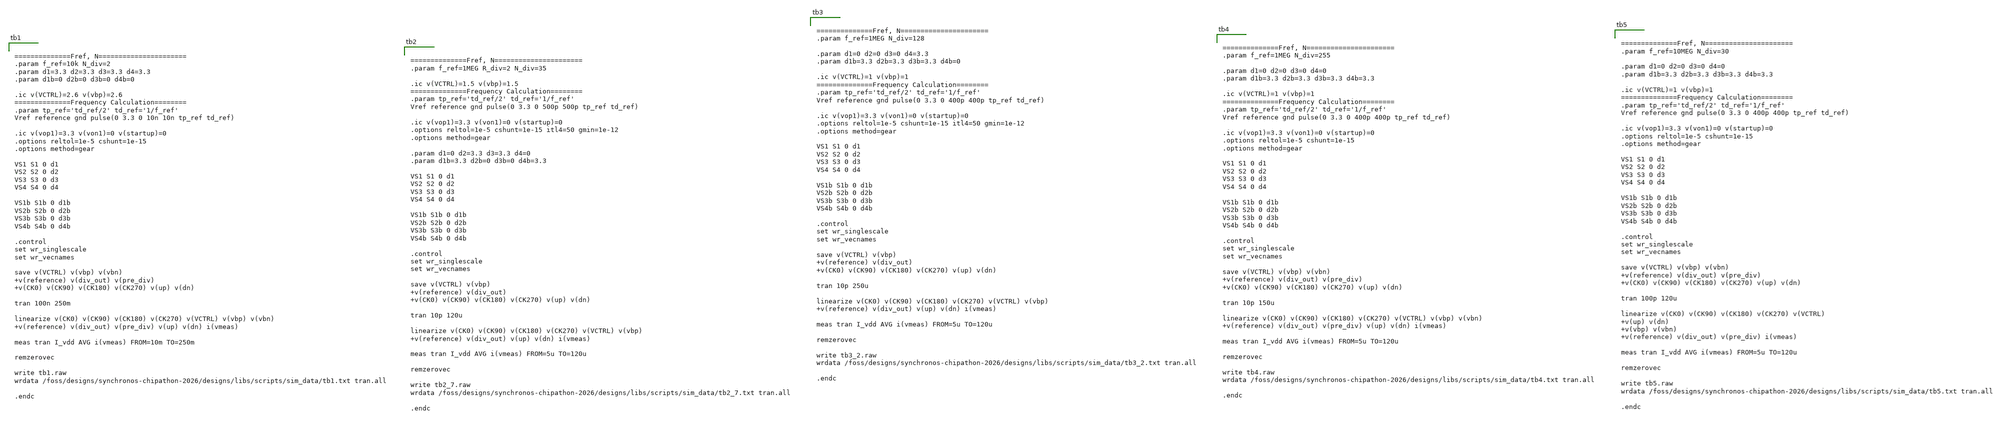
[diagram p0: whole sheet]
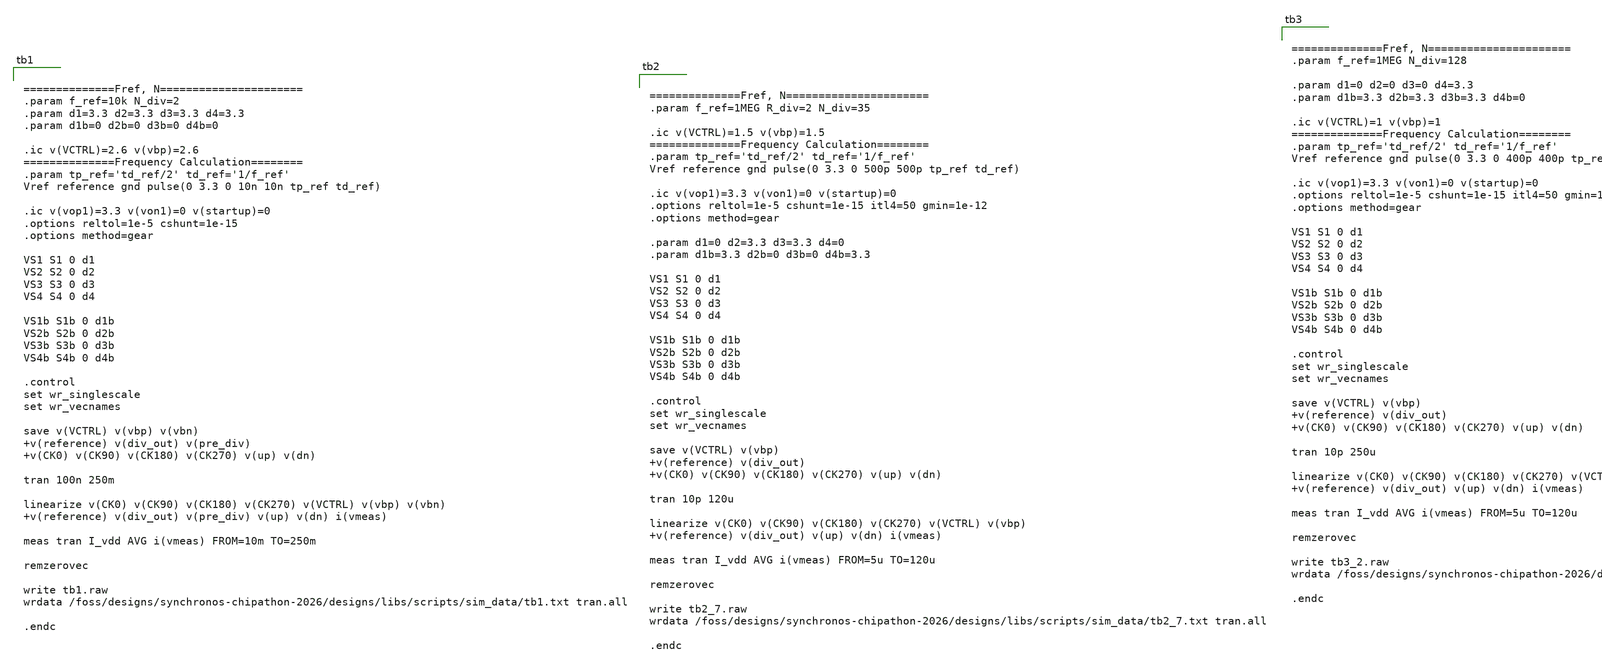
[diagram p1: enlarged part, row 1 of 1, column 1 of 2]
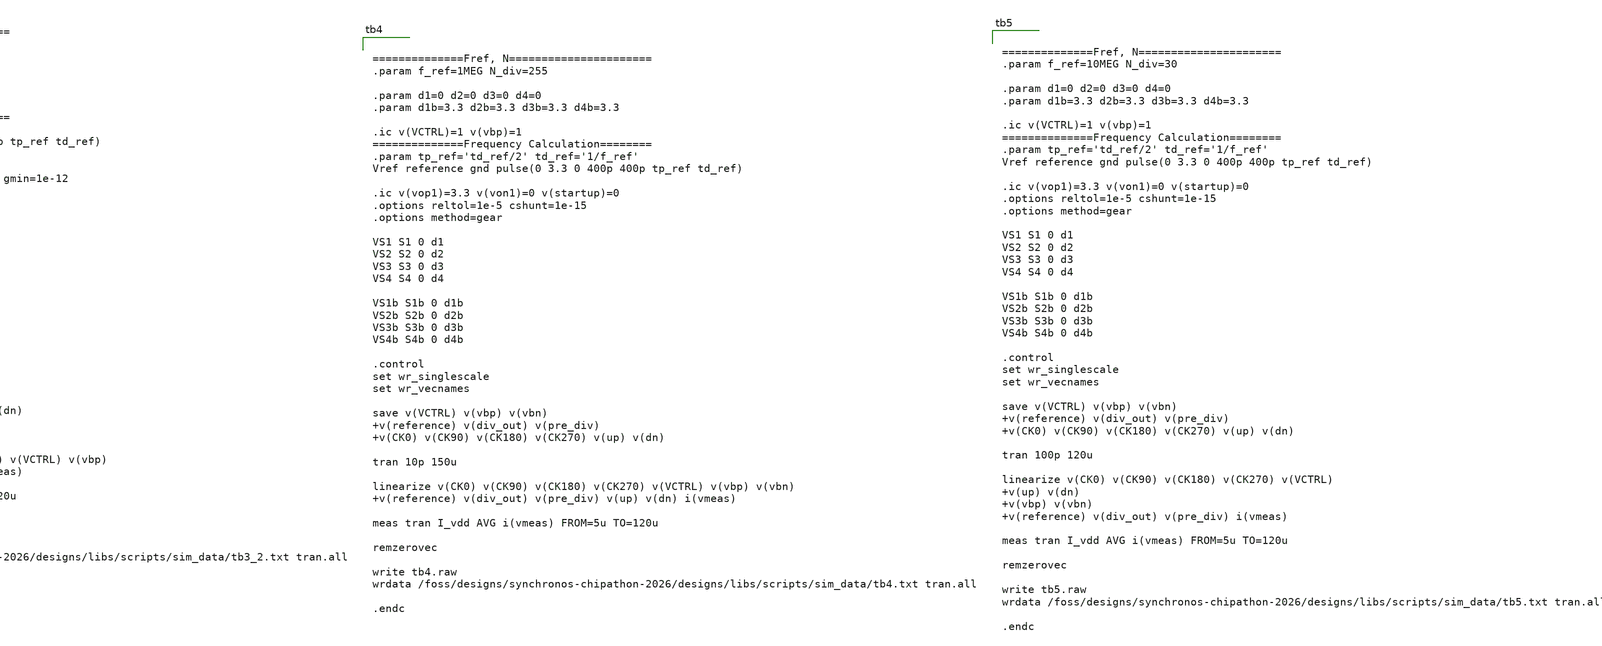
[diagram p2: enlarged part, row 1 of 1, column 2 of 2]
** sch_path: designs/libs/tb_pll/tb_scripts.sch
**.subckt tb_scripts
**** begin user architecture code


==============Fref, N======================
.param f_ref=10k N_div=2
.param d1=3.3 d2=3.3 d3=3.3 d4=3.3
.param d1b=0 d2b=0 d3b=0 d4b=0

.ic v(VCTRL)=2.6 v(vbp)=2.6
==============Frequency Calculation========
.param tp_ref='td_ref/2' td_ref='1/f_ref'
Vref reference gnd pulse(0 3.3 0 10n 10n tp_ref td_ref)

.ic v(vop1)=3.3 v(von1)=0 v(startup)=0
.options reltol=1e-5 cshunt=1e-15
.options method=gear

VS1 S1 0 d1
VS2 S2 0 d2
VS3 S3 0 d3
VS4 S4 0 d4

VS1b S1b 0 d1b
VS2b S2b 0 d2b
VS3b S3b 0 d3b
VS4b S4b 0 d4b

.control
set wr_singlescale
set wr_vecnames

save v(VCTRL) v(vbp) v(vbn) v(reference) v(div_out) v(pre_div) v(CK0) v(CK90) v(CK180) v(CK270)
+ v(up) v(dn)

tran 100n 250m

linearize v(CK0) v(CK90) v(CK180) v(CK270) v(VCTRL) v(vbp) v(vbn) v(reference) v(div_out) v(pre_div)
+ v(up) v(dn) i(vmeas)

meas tran I_vdd AVG i(vmeas) FROM=10m TO=250m

remzerovec

write tb1.raw
wrdata /foss/designs/synchronos-chipathon-2026/designs/libs/scripts/sim_data/tb1.txt tran.all

.endc




==============Fref, N======================
.param f_ref=10MEG N_div=30

.param d1=0 d2=0 d3=0 d4=0
.param d1b=3.3 d2b=3.3 d3b=3.3 d4b=3.3

.ic v(VCTRL)=1 v(vbp)=1
==============Frequency Calculation========
.param tp_ref='td_ref/2' td_ref='1/f_ref'
Vref reference gnd pulse(0 3.3 0 400p 400p tp_ref td_ref)

.ic v(vop1)=3.3 v(von1)=0 v(startup)=0
.options reltol=1e-5 cshunt=1e-15
.options method=gear

VS1 S1 0 d1
VS2 S2 0 d2
VS3 S3 0 d3
VS4 S4 0 d4

VS1b S1b 0 d1b
VS2b S2b 0 d2b
VS3b S3b 0 d3b
VS4b S4b 0 d4b

.control
set wr_singlescale
set wr_vecnames

save v(VCTRL) v(vbp) v(vbn) v(reference) v(div_out) v(pre_div) v(CK0) v(CK90) v(CK180) v(CK270)
+ v(up) v(dn)

tran 100p 120u

linearize v(CK0) v(CK90) v(CK180) v(CK270) v(VCTRL) v(up) v(dn) v(vbp) v(vbn) v(reference)
+ v(div_out) v(pre_div) i(vmeas)

meas tran I_vdd AVG i(vmeas) FROM=5u TO=120u

remzerovec

write tb5.raw
wrdata /foss/designs/synchronos-chipathon-2026/designs/libs/scripts/sim_data/tb5.txt tran.all

.endc




==============Fref, N======================
.param f_ref=1MEG N_div=255

.param d1=0 d2=0 d3=0 d4=0
.param d1b=3.3 d2b=3.3 d3b=3.3 d4b=3.3

.ic v(VCTRL)=1 v(vbp)=1
==============Frequency Calculation========
.param tp_ref='td_ref/2' td_ref='1/f_ref'
Vref reference gnd pulse(0 3.3 0 400p 400p tp_ref td_ref)

.ic v(vop1)=3.3 v(von1)=0 v(startup)=0
.options reltol=1e-5 cshunt=1e-15
.options method=gear

VS1 S1 0 d1
VS2 S2 0 d2
VS3 S3 0 d3
VS4 S4 0 d4

VS1b S1b 0 d1b
VS2b S2b 0 d2b
VS3b S3b 0 d3b
VS4b S4b 0 d4b

.control
set wr_singlescale
set wr_vecnames

save v(VCTRL) v(vbp) v(vbn) v(reference) v(div_out) v(pre_div) v(CK0) v(CK90) v(CK180) v(CK270)
+ v(up) v(dn)

tran 10p 150u

linearize v(CK0) v(CK90) v(CK180) v(CK270) v(VCTRL) v(vbp) v(vbn) v(reference) v(div_out) v(pre_div)
+ v(up) v(dn) i(vmeas)

meas tran I_vdd AVG i(vmeas) FROM=5u TO=120u

remzerovec

write tb4.raw
wrdata /foss/designs/synchronos-chipathon-2026/designs/libs/scripts/sim_data/tb4.txt tran.all

.endc




==============Fref, N======================
.param f_ref=1MEG R_div=2 N_div=35

.ic v(VCTRL)=1.5 v(vbp)=1.5
==============Frequency Calculation========
.param tp_ref='td_ref/2' td_ref='1/f_ref'
Vref reference gnd pulse(0 3.3 0 500p 500p tp_ref td_ref)

.ic v(vop1)=3.3 v(von1)=0 v(startup)=0
.options reltol=1e-5 cshunt=1e-15 itl4=50 gmin=1e-12
.options method=gear

.param d1=0 d2=3.3 d3=3.3 d4=0
.param d1b=3.3 d2b=0 d3b=0 d4b=3.3

VS1 S1 0 d1
VS2 S2 0 d2
VS3 S3 0 d3
VS4 S4 0 d4

VS1b S1b 0 d1b
VS2b S2b 0 d2b
VS3b S3b 0 d3b
VS4b S4b 0 d4b

.control
set wr_singlescale
set wr_vecnames

save v(VCTRL) v(vbp) v(reference) v(div_out) v(CK0) v(CK90) v(CK180) v(CK270) v(up) v(dn)

tran 10p 120u

linearize v(CK0) v(CK90) v(CK180) v(CK270) v(VCTRL) v(vbp) v(reference) v(div_out) v(up) v(dn)
+ i(vmeas)

meas tran I_vdd AVG i(vmeas) FROM=5u TO=120u

remzerovec

write tb2_7.raw
wrdata /foss/designs/synchronos-chipathon-2026/designs/libs/scripts/sim_data/tb2_7.txt tran.all

.endc




==============Fref, N======================
.param f_ref=1MEG N_div=128

.param d1=0 d2=0 d3=0 d4=3.3
.param d1b=3.3 d2b=3.3 d3b=3.3 d4b=0

.ic v(VCTRL)=1 v(vbp)=1
==============Frequency Calculation========
.param tp_ref='td_ref/2' td_ref='1/f_ref'
Vref reference gnd pulse(0 3.3 0 400p 400p tp_ref td_ref)

.ic v(vop1)=3.3 v(von1)=0 v(startup)=0
.options reltol=1e-5 cshunt=1e-15 itl4=50 gmin=1e-12
.options method=gear

VS1 S1 0 d1
VS2 S2 0 d2
VS3 S3 0 d3
VS4 S4 0 d4

VS1b S1b 0 d1b
VS2b S2b 0 d2b
VS3b S3b 0 d3b
VS4b S4b 0 d4b

.control
set wr_singlescale
set wr_vecnames

save v(VCTRL) v(vbp) v(reference) v(div_out) v(CK0) v(CK90) v(CK180) v(CK270) v(up) v(dn)

tran 10p 250u

linearize v(CK0) v(CK90) v(CK180) v(CK270) v(VCTRL) v(vbp) v(reference) v(div_out) v(up) v(dn)
+ i(vmeas)

meas tran I_vdd AVG i(vmeas) FROM=5u TO=120u

remzerovec

write tb3_2.raw
wrdata /foss/designs/synchronos-chipathon-2026/designs/libs/scripts/sim_data/tb3_2.txt tran.all

.endc


**** end user architecture code
**.ends
.end
